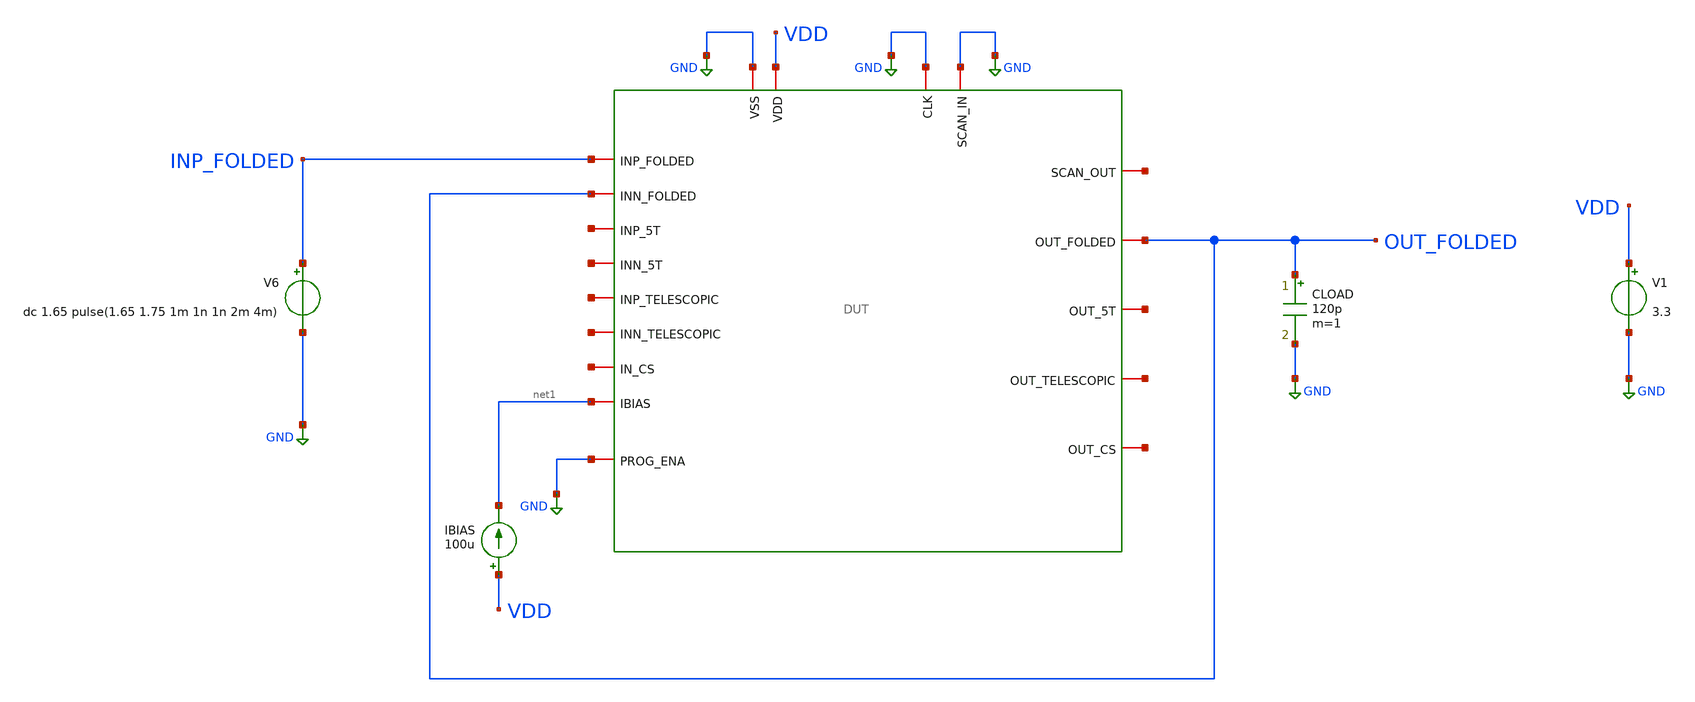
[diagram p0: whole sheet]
** sch_path: designs/libs/pex/folded/step_response/default_step_folded.sch
**.subckt default_step_folded
V1 VDD GND 3.3
CLOAD OUT_FOLDED GND 120p m=1
V6 INP_FOLDED GND dc 1.65 pulse(1.65 1.75 1m 1n 1n 2m 4m)
IBIAS VDD net1 100u
x1 GND net2 GND GND VDD OUT_FOLDED INP_FOLDED net3 net1 OUT_FOLDED net4 net5 net6 net7 net8 net9
+ net10 GND DUT
**** begin user architecture code

.include $::180MCU_MODELS/design.ngspice
.lib $::180MCU_MODELS/sm141064.ngspice typical



.include /foss/designs/libs/pex/DUT.spice
.control
tran 1u 5m

plot v(out_folded) v(inp_folded)

meas tran v_before find v(out_folded) at=0.99m
meas tran v_after find v(out_folded) at=2.5m

let delta = v_after - v_before
let t20_val = v_before + 0.2 * delta
let t80_val = v_before + 0.8 * delta

meas tran t_20 when v(out_folded) = t20_val rise = 1
meas tran t_80 when v(out_folded) = t80_val rise = 1
let sr_rise = delta / (t_80 - t_20)
print sr_rise

meas tran t_20f when v(out_folded) = t80_val fall = 1
meas tran t_80f when v(out_folded) = t20_val fall = 1
let sr_fall = delta / (t_80f - t_20f)
print sr_fall

meas tran vpeak max v(out_folded) from=1m to=3m
let overshoot = (vpeak - v_after) / delta * 100
print overshoot

meas tran t_settle when v(out_folded) = v_after td = 1m rise = 1
let settling = t_settle - 1m
print settling

print v_before v_after delta
.endc


**** end user architecture code
**.ends
.GLOBAL GND
.end
